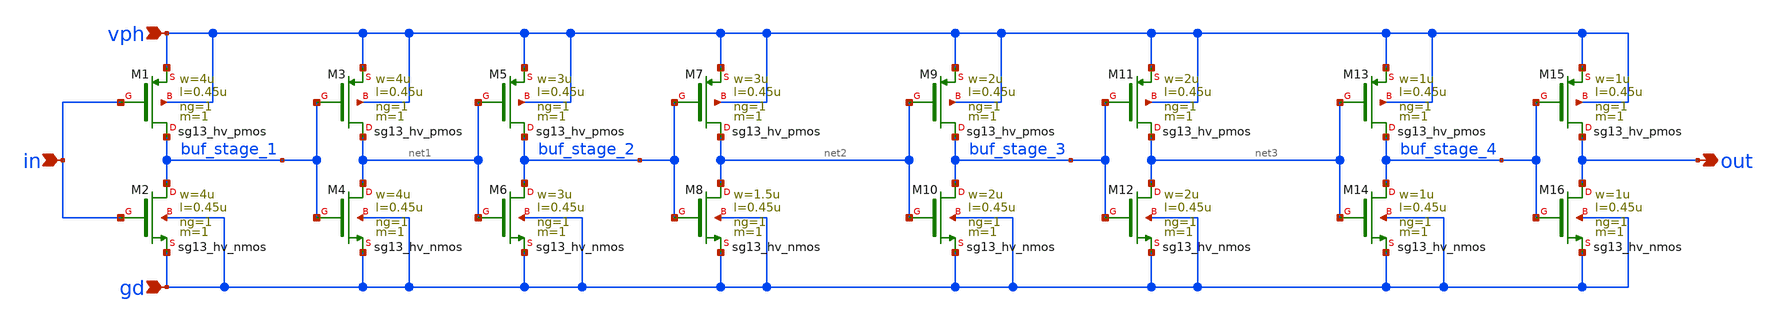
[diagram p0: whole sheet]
** sch_path: schematics/misc/buffer_hv.sch
**.subckt buffer_hv in out vph gd
*.ipin in
*.opin out
*.ipin vph
*.ipin gd
XM1 buf_stage_1 in vph vph sg13_hv_pmos w=4u l=0.45u ng=1 m=1 mm_ok=1
XM2 buf_stage_1 in gd gd sg13_hv_nmos w=4u l=0.45u ng=1 m=1 mm_ok=1
XM3 net1 buf_stage_1 vph vph sg13_hv_pmos w=4u l=0.45u ng=1 m=1 mm_ok=1
XM4 net1 buf_stage_1 gd gd sg13_hv_nmos w=4u l=0.45u ng=1 m=1 mm_ok=1
XM5 buf_stage_2 net1 vph vph sg13_hv_pmos w=3u l=0.45u ng=1 m=1 mm_ok=1
XM6 buf_stage_2 net1 gd gd sg13_hv_nmos w=3u l=0.45u ng=1 m=1 mm_ok=1
XM7 net2 buf_stage_2 vph vph sg13_hv_pmos w=3u l=0.45u ng=1 m=1 mm_ok=1
XM8 net2 buf_stage_2 gd gd sg13_hv_nmos w=1.5u l=0.45u ng=1 m=1 mm_ok=1
XM9 buf_stage_3 net2 vph vph sg13_hv_pmos w=2u l=0.45u ng=1 m=1 mm_ok=1
XM10 buf_stage_3 net2 gd gd sg13_hv_nmos w=2u l=0.45u ng=1 m=1 mm_ok=1
XM11 net3 buf_stage_3 vph vph sg13_hv_pmos w=2u l=0.45u ng=1 m=1 mm_ok=1
XM12 net3 buf_stage_3 gd gd sg13_hv_nmos w=2u l=0.45u ng=1 m=1 mm_ok=1
XM13 buf_stage_4 net3 vph vph sg13_hv_pmos w=1u l=0.45u ng=1 m=1 mm_ok=1
XM14 buf_stage_4 net3 gd gd sg13_hv_nmos w=1u l=0.45u ng=1 m=1 mm_ok=1
XM15 out buf_stage_4 vph vph sg13_hv_pmos w=1u l=0.45u ng=1 m=1 mm_ok=1
XM16 out buf_stage_4 gd gd sg13_hv_nmos w=1u l=0.45u ng=1 m=1 mm_ok=1
**.ends
.end
